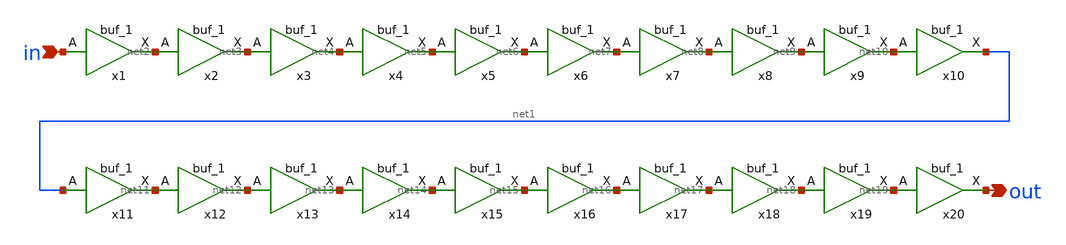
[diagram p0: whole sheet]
** sch_path: designs/pmu_design/delay_chain/1-schematics/buf20_1.sch
**.subckt buf20_1 in out
*.ipin in
*.opin out
x1 in VGND VNB VPB VPWR net2 sky130_fd_sc_hd__buf_1
x2 net2 VGND VNB VPB VPWR net3 sky130_fd_sc_hd__buf_1
x3 net3 VGND VNB VPB VPWR net4 sky130_fd_sc_hd__buf_1
x4 net4 VGND VNB VPB VPWR net5 sky130_fd_sc_hd__buf_1
x5 net5 VGND VNB VPB VPWR net6 sky130_fd_sc_hd__buf_1
x6 net6 VGND VNB VPB VPWR net7 sky130_fd_sc_hd__buf_1
x7 net7 VGND VNB VPB VPWR net8 sky130_fd_sc_hd__buf_1
x8 net8 VGND VNB VPB VPWR net9 sky130_fd_sc_hd__buf_1
x9 net9 VGND VNB VPB VPWR net10 sky130_fd_sc_hd__buf_1
x10 net10 VGND VNB VPB VPWR net1 sky130_fd_sc_hd__buf_1
x11 net1 VGND VNB VPB VPWR net11 sky130_fd_sc_hd__buf_1
x12 net11 VGND VNB VPB VPWR net12 sky130_fd_sc_hd__buf_1
x13 net12 VGND VNB VPB VPWR net13 sky130_fd_sc_hd__buf_1
x14 net13 VGND VNB VPB VPWR net14 sky130_fd_sc_hd__buf_1
x15 net14 VGND VNB VPB VPWR net15 sky130_fd_sc_hd__buf_1
x16 net15 VGND VNB VPB VPWR net16 sky130_fd_sc_hd__buf_1
x17 net16 VGND VNB VPB VPWR net17 sky130_fd_sc_hd__buf_1
x18 net17 VGND VNB VPB VPWR net18 sky130_fd_sc_hd__buf_1
x19 net18 VGND VNB VPB VPWR net19 sky130_fd_sc_hd__buf_1
x20 net19 VGND VNB VPB VPWR out sky130_fd_sc_hd__buf_1
**.ends
.end
